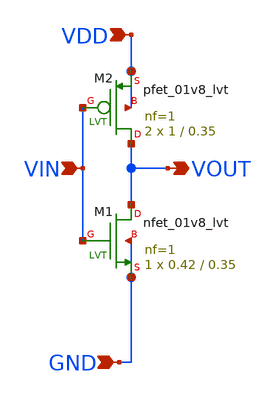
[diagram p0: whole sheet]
** sch_path: design/LELO_SVOD_SKY130A/LELO_INV.sch
**.subckt LELO_INV VIN VDD GND VOUT
*.ipin VIN
*.ipin VDD
*.ipin GND
*.opin VOUT
XM1 VOUT VIN GND GND sky130_fd_pr__nfet_01v8_lvt L=0.35 W=0.42 nf=1 ad='int((1 + 1)/2) * 0.42 / 1 * 0.29'
+ as='int((1 + 2)/2) * 0.42 / 1 * 0.29' pd='2*int((1 + 1)/2) * (0.42 / 1 + 0.29)' ps='2*int((1 + 2)/2) * (0.42 / 1 + 0.29)'
+ nrd='0.29 / 0.42 ' nrs='0.29 / 0.42 ' sa=0 sb=0 sd=0 mult=1 m=1
XM2 VOUT VIN VDD VDD sky130_fd_pr__pfet_01v8_lvt L=0.35 W=1 nf=1 ad='int((1 + 1)/2) * 1 / 1 * 0.29' as='int((1 + 2)/2) * 1 / 1 * 0.29'
+ pd='2*int((1 + 1)/2) * (1 / 1 + 0.29)' ps='2*int((1 + 2)/2) * (1 / 1 + 0.29)' nrd='0.29 / 1 ' nrs='0.29 / 1 '
+ sa=0 sb=0 sd=0 mult=2 m=2
**.ends
.end
